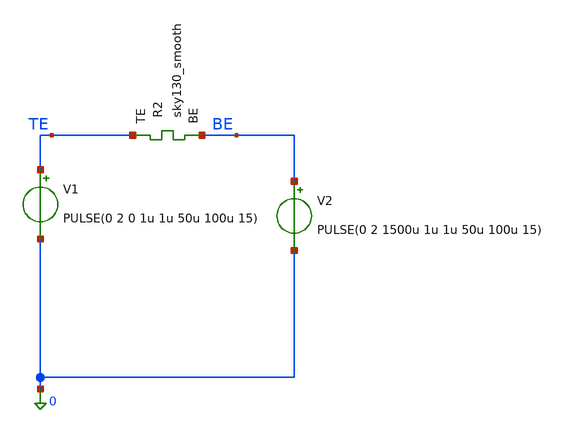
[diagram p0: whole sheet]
** sch_path: memristor_models/sky130_smooth/tb_pulses_smooth.sch
**.subckt tb_pulses_smooth
V1 TE 0 PULSE(0 2 0 1u 1u 50u 100u 15)
XR2 TE BE sky130_smooth Tfilament_0=3.3e-9
V2 BE 0 PULSE(0 2 1500u 1u 1u 50u 100u 15)
**** begin user architecture code

** opencircuitdesign pdks install
.inc $::SKYWATER_MODELS/sky130_smooth.spice



.option savecurrents
.tran 1u 3m
.control
	save all
	run
	write tb_pulses_smooth.raw
.endc



**** end user architecture code
**.ends
.end
